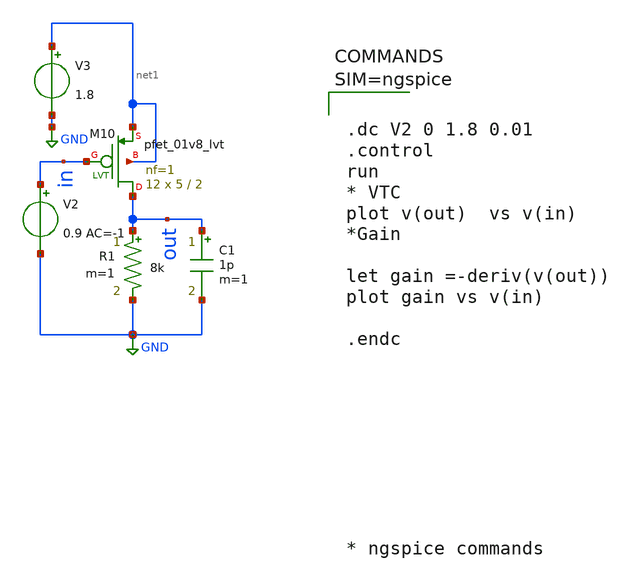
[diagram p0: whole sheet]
** sch_path: spice/mos_rcload.sch
**.subckt mos_rcload
V2 in GND 0.9 AC=-1
V3 net1 GND 1.8
XM10 out in net1 net1 sky130_fd_pr__pfet_01v8_lvt L=2 W=5 nf=1 ad='int((1 + 1)/2) * 5 / 1 * 0.29' as='int((1 + 2)/2) * 5 / 1 * 0.29'
+ pd='2*int((1 + 1)/2) * (5 / 1 + 0.29)' ps='2*int((1 + 2)/2) * (5 / 1 + 0.29)' nrd='0.29 / 5 ' nrs='0.29 / 5 '
+ sa=0 sb=0 sd=0 mult=12 m=12
R1 out GND 8k m=1
C1 out GND 1p m=1
**** begin user architecture code

** opencircuitdesign pdks install
.lib $::SKYWATER_MODELS/sky130.lib.spice tt




.dc V2 0 1.8 0.01
.control
run
* VTC
plot v(out)  vs v(in)
*Gain

let gain =-deriv(v(out))
plot gain vs v(in)

.endc









* ngspice commands



**** end user architecture code
**.ends
.GLOBAL GND
.end
